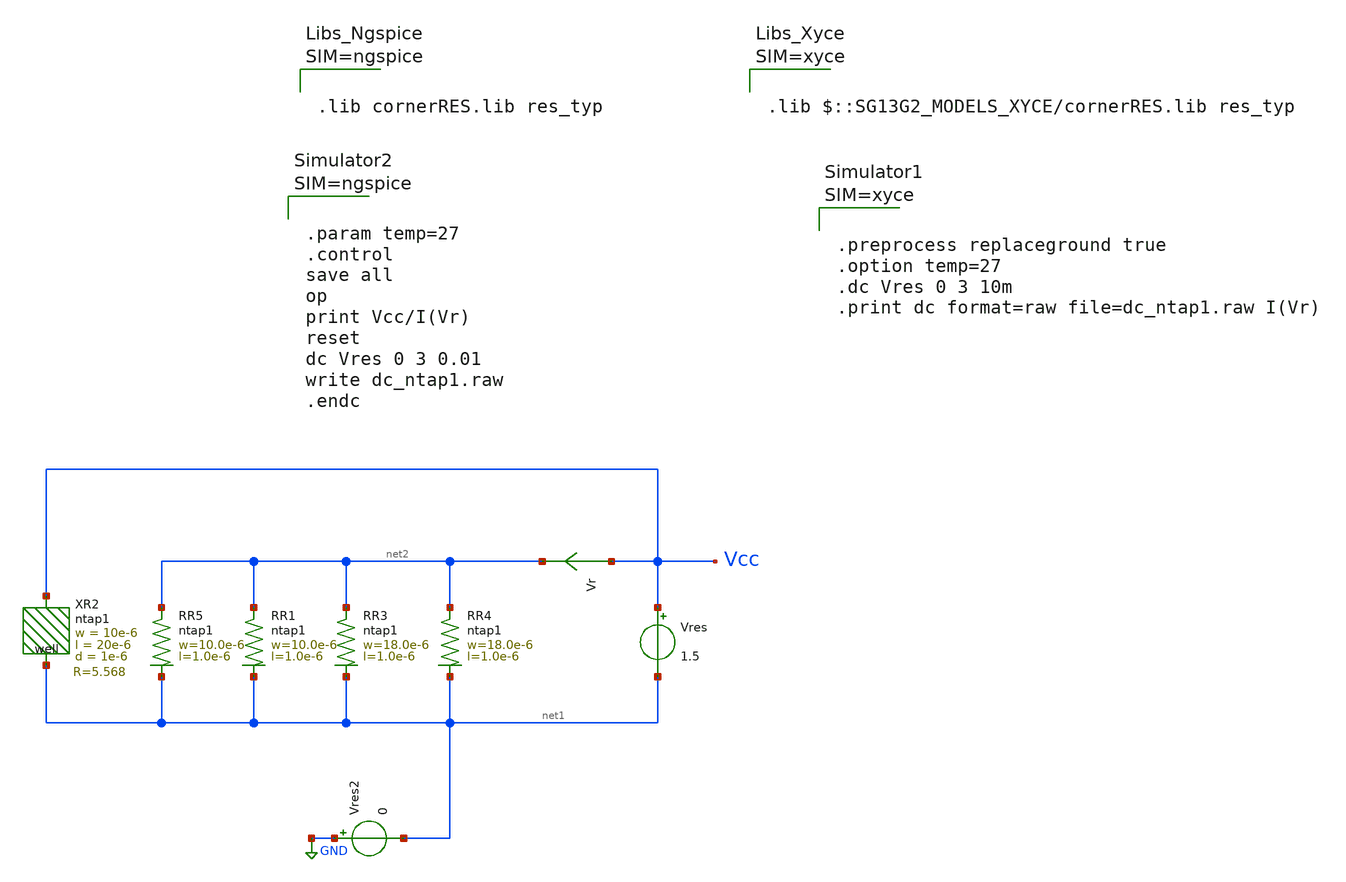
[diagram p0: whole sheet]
** sch_path: ihp-sg13g2/libs.tech/xschem/sg13g2_tests_xyce/dc_ntap1.sch
* Copyright 2023 IHP PDK Authors
**.subckt dc_ntap1
Vres Vcc net1 1.5
Vr Vcc net2 0
.save i(vr)
Vres2 GND net1 0
XR1 net2 net1 ntap1 R=30.62 w=10.0e-6 l=1.0e-6
XR4 net2 net1 ntap1 R=17.5 w=18.0e-6 l=1.0e-6
XR5 net2 net1 ntap1 R=30.62 w=10.0e-6 l=1.0e-6
XR3 net2 net1 ntap1 R=17.5 w=18.0e-6 l=1.0e-6
XR2 Vcc net1 ntap1 R=5.568 w=10e-6 l=20e-6 d=1e-6
**** begin user architecture code









.lib cornerRES.lib res_typ






.param temp=27
.control
save all
op
print Vcc/I(Vr)
reset
dc Vres 0 3 0.01
write dc_ntap1.raw
.endc



**** end user architecture code
**.ends
.GLOBAL GND
.end
